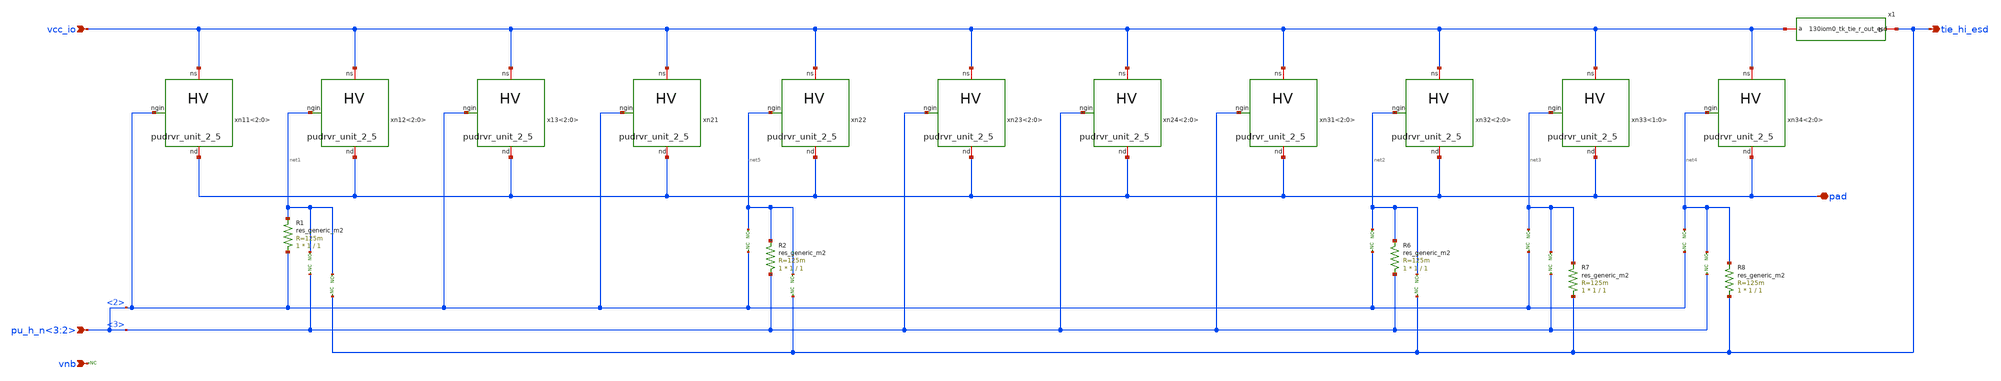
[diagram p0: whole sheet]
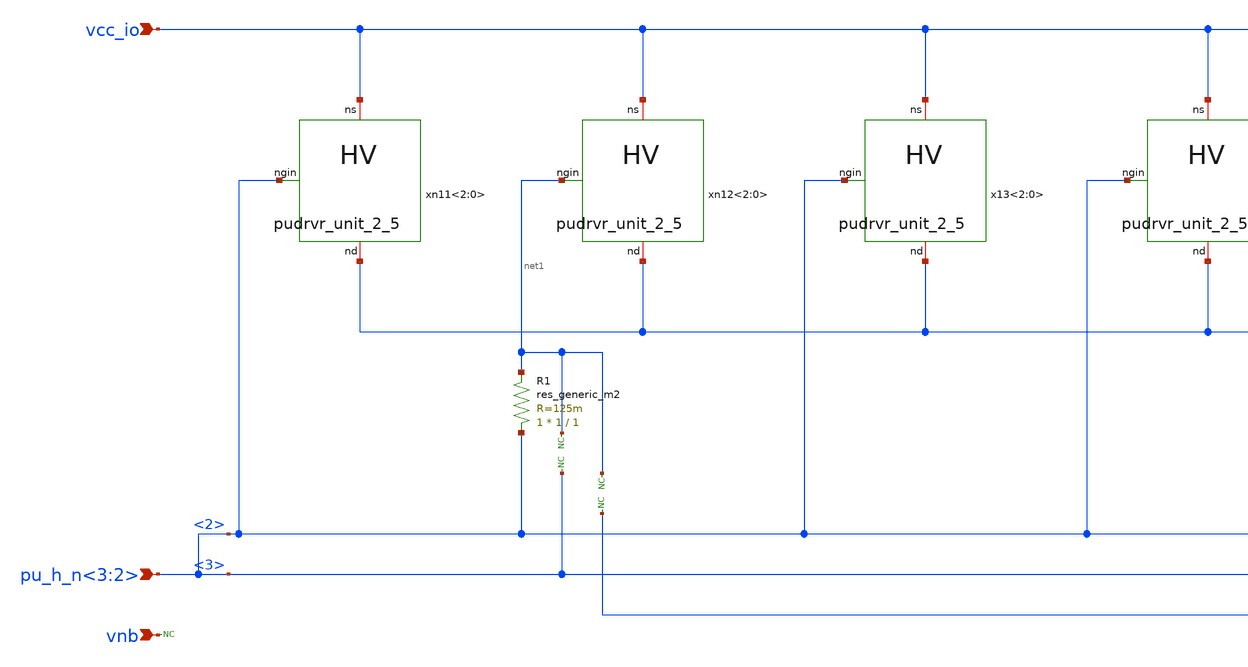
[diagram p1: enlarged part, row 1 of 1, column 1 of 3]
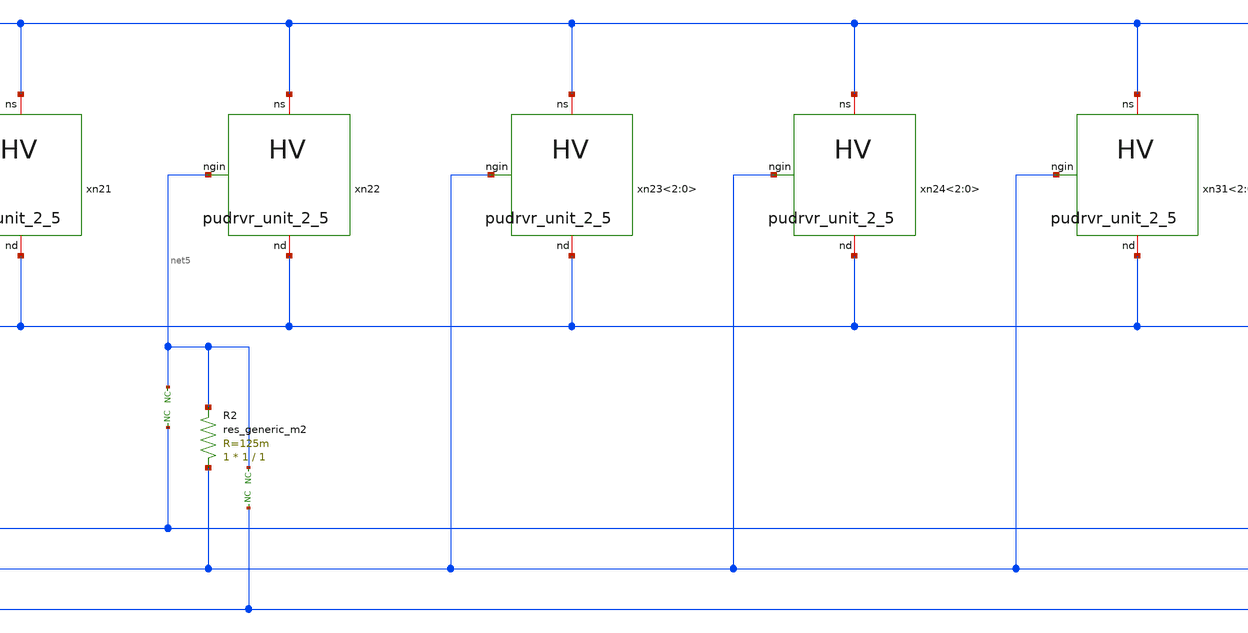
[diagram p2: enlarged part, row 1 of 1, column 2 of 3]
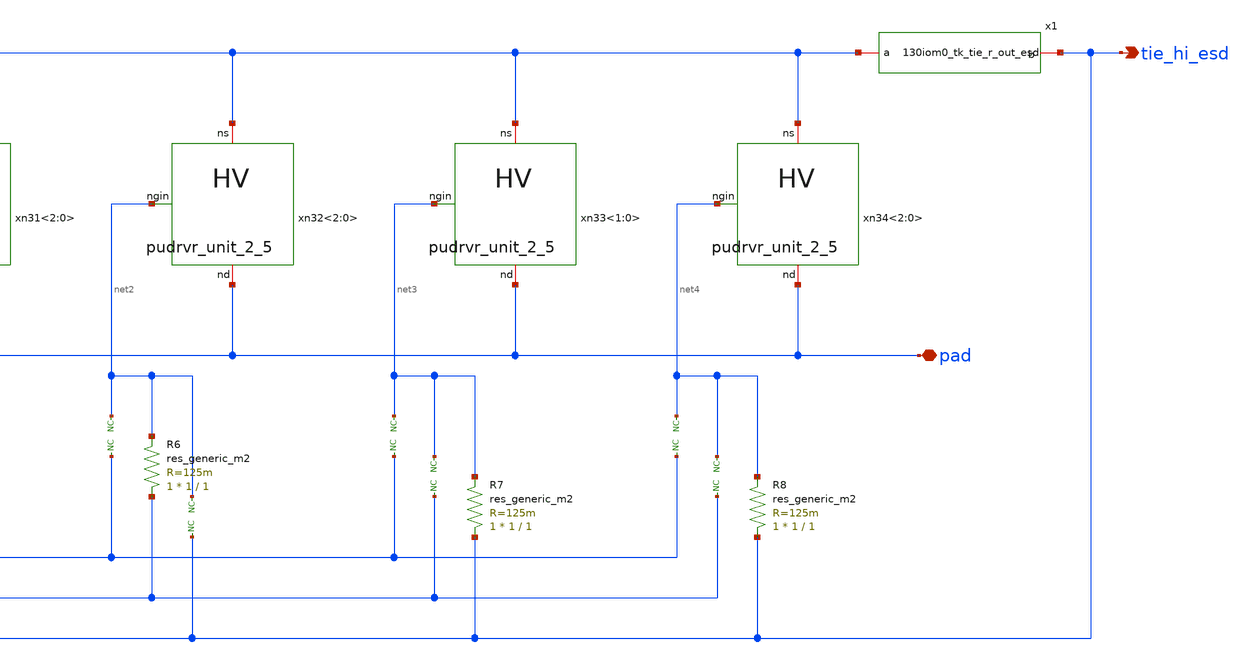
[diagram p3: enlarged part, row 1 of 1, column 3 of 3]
** sch_path: pudrvr_strong.sch
**.subckt pudrvr_strong vcc_io pad pu_h_n<3:2> vnb tie_hi_esd
*.ipin vcc_io
*.iopin pad
*.ipin pu_h_n<3:2>
*.ipin vnb
*.opin tie_hi_esd
* noconn vnb
x1 vcc_io tie_hi_esd 130iom0_tk_tie_r_out_esd
R1 pu_h_n<3:2> net1 sky130_fd_pr__res_generic_m2 W=1 L=1 m=1
* noconn pu_h_n<3:2>
* noconn #net1
* noconn tie_hi_esd
* noconn #net1
R6 pu_h_n<3:2> net2 sky130_fd_pr__res_generic_m2 W=1 L=1 m=1
* noconn pu_h_n<3:2>
* noconn #net2
* noconn tie_hi_esd
* noconn #net2
R7 tie_hi_esd net3 sky130_fd_pr__res_generic_m2 W=1 L=1 m=1
* noconn pu_h_n<3:2>
* noconn #net3
* noconn pu_h_n<3:2>
* noconn #net3
R8 tie_hi_esd net4 sky130_fd_pr__res_generic_m2 W=1 L=1 m=1
* noconn pu_h_n<3:2>
* noconn #net4
* noconn pu_h_n<3:2>
* noconn #net4
xn11<2:0> pad pu_h_n<3:2> vcc_io pudrvr_unit_2_5
xn12<2:0> pad net1 vcc_io pudrvr_unit_2_5
x13<2:0> pad pu_h_n<3:2> vcc_io pudrvr_unit_2_5
xn21 pad pu_h_n<3:2> vcc_io pudrvr_unit_2_5
xn22 pad net5 vcc_io pudrvr_unit_2_5
xn23<2:0> pad pu_h_n<3:2> vcc_io pudrvr_unit_2_5
xn24<2:0> pad pu_h_n<3:2> vcc_io pudrvr_unit_2_5
xn31<2:0> pad pu_h_n<3:2> vcc_io pudrvr_unit_2_5
xn32<2:0> pad net2 vcc_io pudrvr_unit_2_5
xn33<1:0> pad net3 vcc_io pudrvr_unit_2_5
xn34<2:0> pad net4 vcc_io pudrvr_unit_2_5
R2 pu_h_n<3:2> net5 sky130_fd_pr__res_generic_m2 W=1 L=1 m=1
* noconn pu_h_n<3:2>
* noconn #net5
* noconn tie_hi_esd
* noconn #net5
**.ends

* expanding   symbol:  130iom0_tk_tie_r_out_esd.sym # of pins=2
** sym_path: 130iom0_tk_tie_r_out_esd.sym
** sch_path: 130iom0_tk_tie_r_out_esd.sch
.subckt 130iom0_tk_tie_r_out_esd a b
*.iopin a
*.iopin b
Xresd_r b a sky130_fd_pr__rpoly W=0.5 L=10.2 m=1
.ends


* expanding   symbol:  pudrvr_unit_2_5.sym # of pins=3
** sym_path: pudrvr_unit_2_5.sym
** sch_path: pudrvr_unit_2_5.sch
.subckt pudrvr_unit_2_5 nd ngin ns
*.iopin nd
*.iopin ns
*.ipin ngin
XM1 nd ngin ns ns sky130_fd_pr__nfet_05v0_nvt L=0.6 W=5 nf=1 ad='int((nf+1)/2) * W/nf * 0.29' as='int((nf+2)/2) * W/nf * 0.29'
+ pd='2*int((nf+1)/2) * (W/nf + 0.29)' ps='2*int((nf+2)/2) * (W/nf + 0.29)' nrd='0.29 / W' nrs='0.29 / W'
+ sa=0 sb=0 sd=0 mult=2 m=2
.ends

.end
